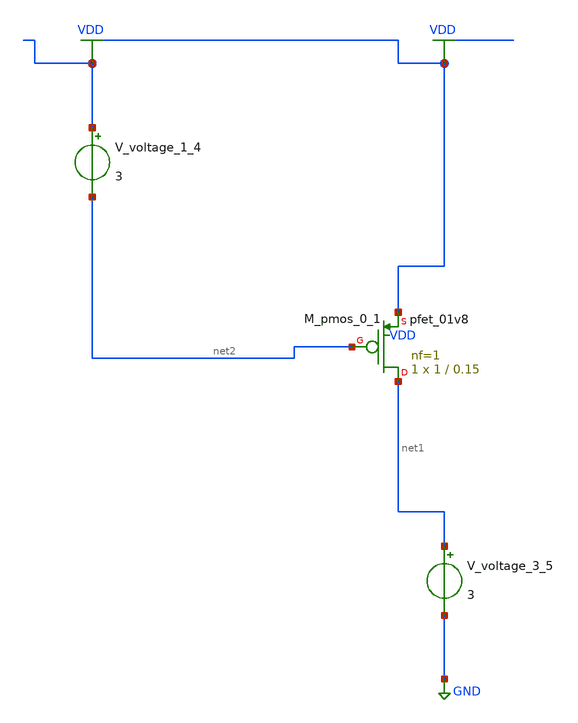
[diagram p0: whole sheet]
** sch_path: schematics/AMSNet/23.sch
**.subckt 23
XM_pmos_0_1 net1 net2 VDD VDD sky130_fd_pr__pfet_01v8 L=0.15 W=1 nf=1 ad='int((1 + 1)/2) * 1 / 1 * 0.29'
+ as='int((1 + 2)/2) * 1 / 1 * 0.29' pd='2*int((1 + 1)/2) * (1 / 1 + 0.29)' ps='2*int((1 + 2)/2) * (1 / 1 + 0.29)'
+ nrd='0.29 / 1 ' nrs='0.29 / 1 ' sa=0 sb=0 sd=0 mult=1 m=1
V_voltage_1_4 VDD net2 3
V_voltage_3_5 net1 GND 3
**.ends
.GLOBAL GND
.GLOBAL VDD
.end
